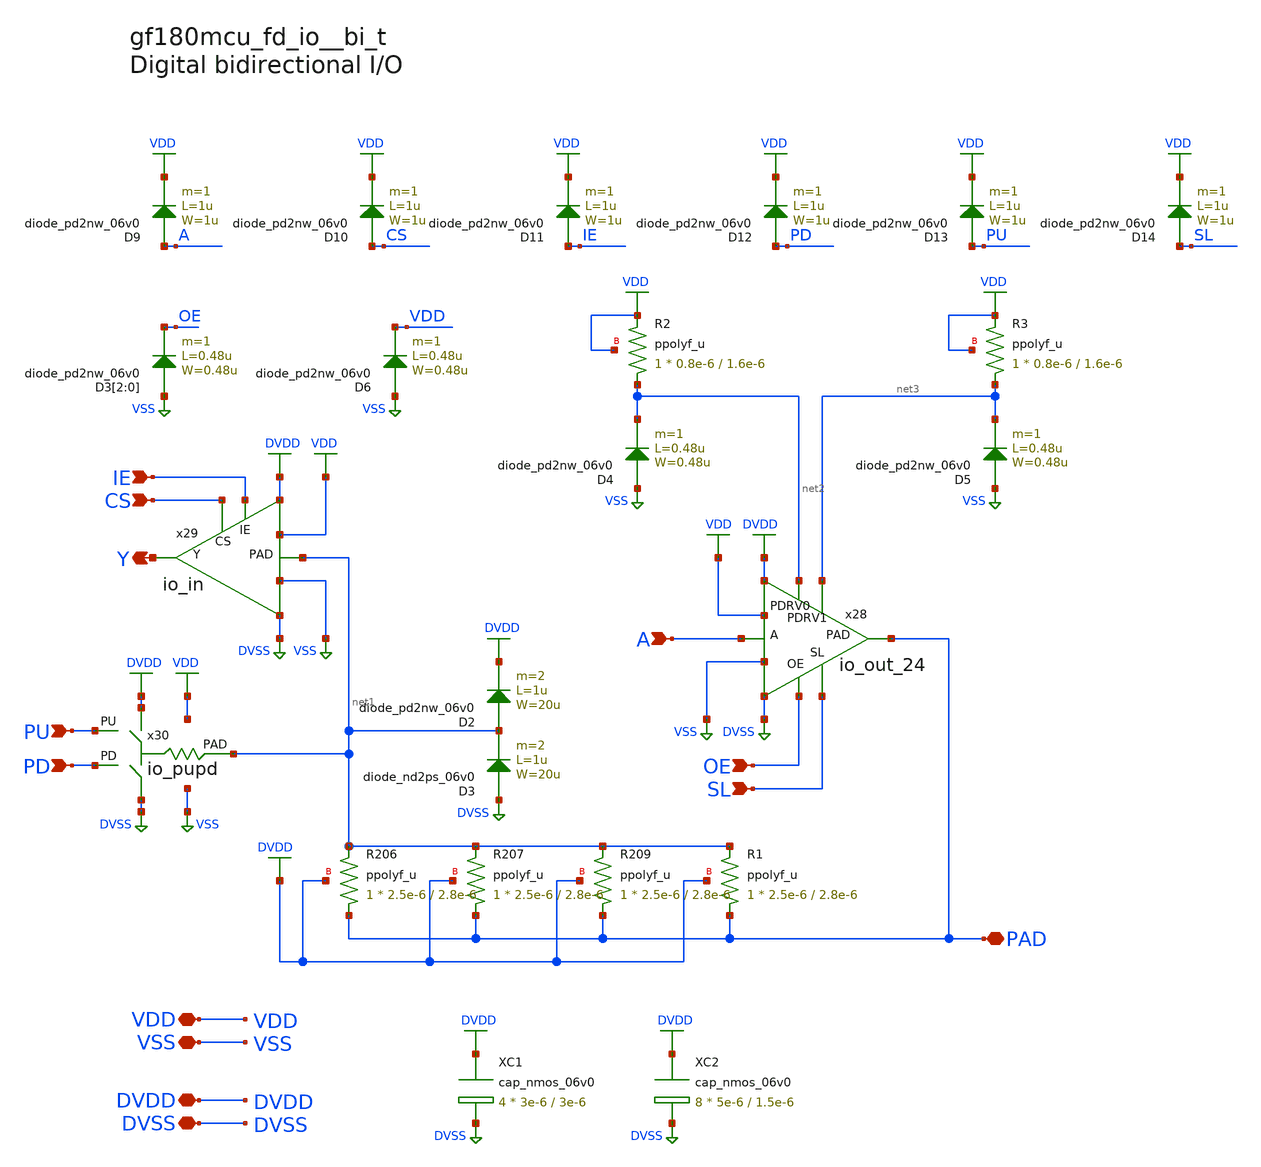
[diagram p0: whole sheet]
** sch_path: cells/bi_24t/gf180mcu_fd_io__bi_24t.sch
* Copyright 2023 David Mitchell Bailey
* Licensed under the Apache License, Version 2.0 (the "License");
* you may not use this file except in compliance with the License.
* You may obtain a copy of the License at
* https://www.apache.org/licenses/LICENSE-2.0
* Unless required by applicable law or agreed to in writing, software
* distributed under the License is distributed on an "AS IS" BASIS,
* WITHOUT WARRANTIES OR CONDITIONS OF ANY KIND, either express or implied.
* See the License for the specific language governing permissions and
* limitations under the License.
**.subckt gf180mcu_fd_io__bi_24t A VDD Y VSS DVDD DVSS PU PD SL OE CS IE PAD
*.ipin A
*.iopin VDD
*.opin Y
*.iopin VSS
*.iopin DVDD
*.iopin DVSS
*.ipin PU
*.ipin PD
*.ipin SL
*.ipin OE
*.ipin CS
*.ipin IE
*.iopin PAD
XR206 PAD net1 DVDD ppolyf_u r_width=2.5e-6 r_length=2.8e-6 m=1
XR207 PAD net1 DVDD ppolyf_u r_width=2.5e-6 r_length=2.8e-6 m=1
XR209 PAD net1 DVDD ppolyf_u r_width=2.5e-6 r_length=2.8e-6 m=1
XR1 PAD net1 DVDD ppolyf_u r_width=2.5e-6 r_length=2.8e-6 m=1
x28 OE A SL PAD DVDD DVSS VDD VSS net2 net3 io_out_24
x29 net1 IE CS Y DVDD DVSS VDD VSS io_in
x30 DVDD DVSS PU PD net1 VDD VSS io_pupd
XC1 DVDD DVSS cap_nmos_06v0 c_width=3e-6 c_length=3e-6 m=4
XC2 DVDD DVSS cap_nmos_06v0 c_width=5e-6 c_length=1.5e-6 m=8
D3 DVSS net1 diode_nd2ps_06v0 area='20u * 1u ' pj='2*20u + 2*1u ' m=2
D2 net1 DVDD diode_pd2nw_06v0 area='20u * 1u ' pj='2*20u + 2*1u ' m=2
D3[2] VSS OE diode_pd2nw_06v0 area='0.48u * 0.48u ' pj='2*0.48u + 2*0.48u ' m=1
D3[1] VSS OE diode_pd2nw_06v0 area='0.48u * 0.48u ' pj='2*0.48u + 2*0.48u ' m=1
D3[0] VSS OE diode_pd2nw_06v0 area='0.48u * 0.48u ' pj='2*0.48u + 2*0.48u ' m=1
D4 VSS net2 diode_pd2nw_06v0 area='0.48u * 0.48u ' pj='2*0.48u + 2*0.48u ' m=1
D5 VSS net3 diode_pd2nw_06v0 area='0.48u * 0.48u ' pj='2*0.48u + 2*0.48u ' m=1
D6 VSS VDD diode_pd2nw_06v0 area='0.48u * 0.48u ' pj='2*0.48u + 2*0.48u ' m=1
D9 A VDD diode_pd2nw_06v0 area='1u * 1u ' pj='2*1u + 2*1u ' m=1
D10 CS VDD diode_pd2nw_06v0 area='1u * 1u ' pj='2*1u + 2*1u ' m=1
D11 IE VDD diode_pd2nw_06v0 area='1u * 1u ' pj='2*1u + 2*1u ' m=1
D12 PD VDD diode_pd2nw_06v0 area='1u * 1u ' pj='2*1u + 2*1u ' m=1
D13 PU VDD diode_pd2nw_06v0 area='1u * 1u ' pj='2*1u + 2*1u ' m=1
D14 SL VDD diode_pd2nw_06v0 area='1u * 1u ' pj='2*1u + 2*1u ' m=1
XR2 net2 VDD VDD ppolyf_u r_width=0.8e-6 r_length=1.6e-6 m=1
XR3 net3 VDD VDD ppolyf_u r_width=0.8e-6 r_length=1.6e-6 m=1
**.ends
.GLOBAL DVSS
.GLOBAL DVDD
.GLOBAL VDD
.GLOBAL VSS
.end
